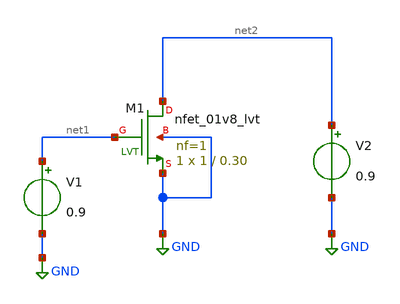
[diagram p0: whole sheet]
** sch_path: Simple-CS-Amplifier/gmid.sch
**.subckt gmid
XM1 net2 net1 GND GND sky130_fd_pr__nfet_01v8_lvt L=0.30 W=1 nf=1 ad='int((nf+1)/2) * W/nf * 0.29' as='int((nf+2)/2) * W/nf * 0.29'
+ pd='2*int((nf+1)/2) * (W/nf + 0.29)' ps='2*int((nf+2)/2) * (W/nf + 0.29)' nrd='0.29 / W' nrs='0.29 / W'
+ sa=0 sb=0 sd=0 mult=1 m=1
V1 net1 GND 0.9
V2 net2 GND 0.9
**** begin user architecture code



.lib /usr/local/share/pdk/sky130A/libs.tech/ngspice/sky130.lib.spice tt
.option wnflag=1 scale=1e-6

.control
save all
save @m.xm1.msky130_fd_pr__nfet_01v8_lvt[id]
save @m.xm1.msky130_fd_pr__nfet_01v8_lvt[gm]
save @m.xm1.msky130_fd_pr__nfet_01v8_lvt[gds]

dc v1 0 1.8 1m

let id = @m.xm1.msky130_fd_pr__nfet_01v8_lvt[id]
let gm = @m.xm1.msky130_fd_pr__nfet_01v8_lvt[gm]
let ro = 1/@m.xm1.msky130_fd_pr__nfet_01v8_lvt[gds]

let gmoverid = gm/id
let vstar = 2/gmoverid

plot id vs vstar

wrdata vstar.txt vstar id

.endc


**** end user architecture code
**.ends
.GLOBAL GND
.end
